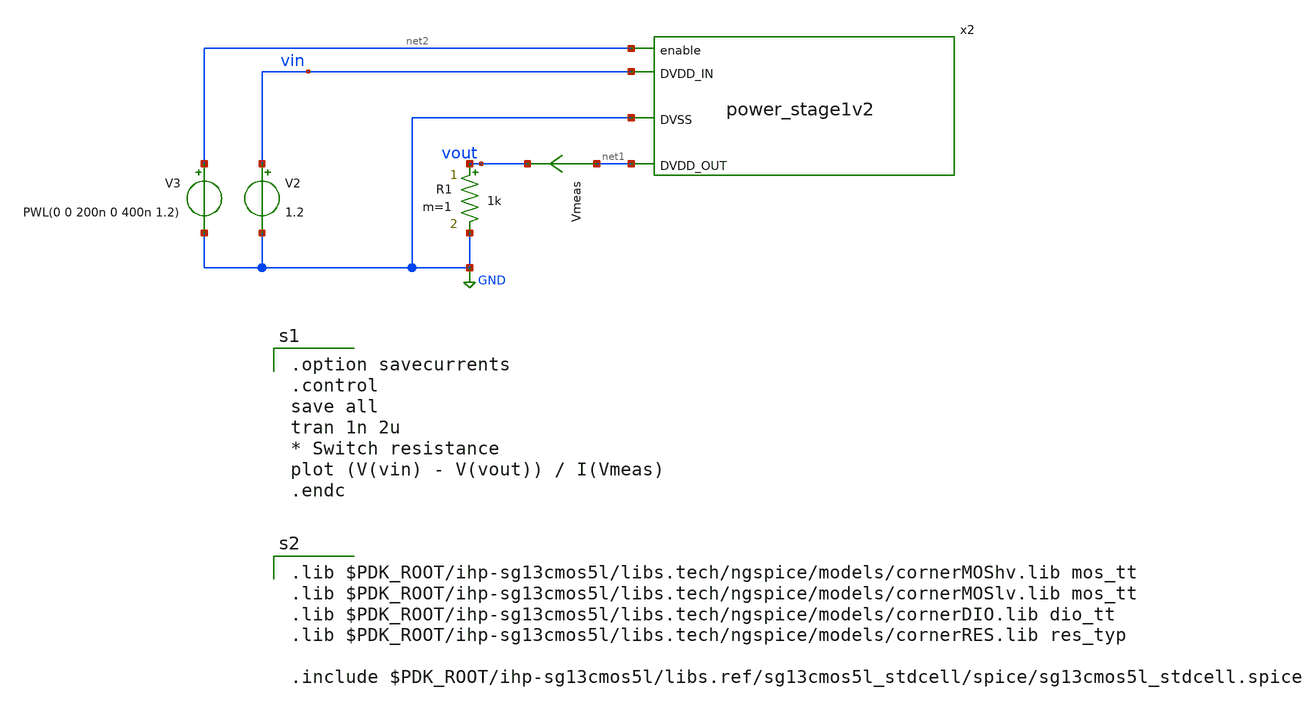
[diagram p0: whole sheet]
** sch_path: xschem/power_stage1v2_tb.sch
**.subckt power_stage1v2_tb
Vmeas net1 vout 0
.save i(vmeas)
R1 vout GND 1k m=1
V2 vin GND 1.2
V3 net2 GND PWL(0 0 200n 0 400n 1.2)
x2 net2 vin GND net1 power_stage1v2
**** begin user architecture code

.option savecurrents
.control
save all
tran 1n 2u
* Switch resistance
plot (V(vin) - V(vout)) / I(Vmeas)
.endc


.lib $PDK_ROOT/ihp-sg13cmos5l/libs.tech/ngspice/models/cornerMOShv.lib mos_tt
.lib $PDK_ROOT/ihp-sg13cmos5l/libs.tech/ngspice/models/cornerMOSlv.lib mos_tt
.lib $PDK_ROOT/ihp-sg13cmos5l/libs.tech/ngspice/models/cornerDIO.lib dio_tt
.lib $PDK_ROOT/ihp-sg13cmos5l/libs.tech/ngspice/models/cornerRES.lib res_typ

.include $PDK_ROOT/ihp-sg13cmos5l/libs.ref/sg13cmos5l_stdcell/spice/sg13cmos5l_stdcell.spice

**** end user architecture code
**.ends

* expanding   symbol:  power_stage1v2.sym # of pins=4
** sym_path: xschem/power_stage1v2.sym
** sch_path: xschem/power_stage1v2.sch
.subckt power_stage1v2 enable DVDD_IN DVSS DVDD_OUT
*.ipin enable
*.ipin DVDD_IN
*.ipin DVSS
*.opin DVDD_OUT
x2 enable P_DRIVE DVDD_IN DVSS gate_drive_1v2
XM1 DVDD_OUT P_DRIVE DVDD_IN DVDD_IN sg13_lv_pmos w=5u l=0.13u ng=1 m=500 mm_ok=1
.ends


* expanding   symbol:  gate_drive_1v2.sym # of pins=4
** sym_path: xschem/gate_drive_1v2.sym
** sch_path: xschem/gate_drive_1v2.sch
.subckt gate_drive_1v2 in out dvdd dvss
*.opin out
*.ipin in
*.iopin dvdd
*.iopin dvss
x2 net1 net3 dvdd dvss sg13cmos5l_inv_2
x3 net2 net1 dvdd dvss sg13cmos5l_inv_8
x4 net4 net2 dvdd dvss sg13cmos5l_inv_16
x6 net3 in dvdd dvss sg13cmos5l_inv_1
x7 in dvdd dvss sg13cmos5l_antennanp
x8[1] dvdd dvss sg13cmos5l_decap_4
x8[0] dvdd dvss sg13cmos5l_decap_4
XM1 out net4 dvss dvss sg13_lv_nmos w=26.64u l=0.13u ng=36 m=1 mm_ok=1
XM2 out net4 dvdd dvdd sg13_lv_pmos w=40.32u l=0.13u ng=36 m=1 mm_ok=1
.ends

.GLOBAL GND
.end
